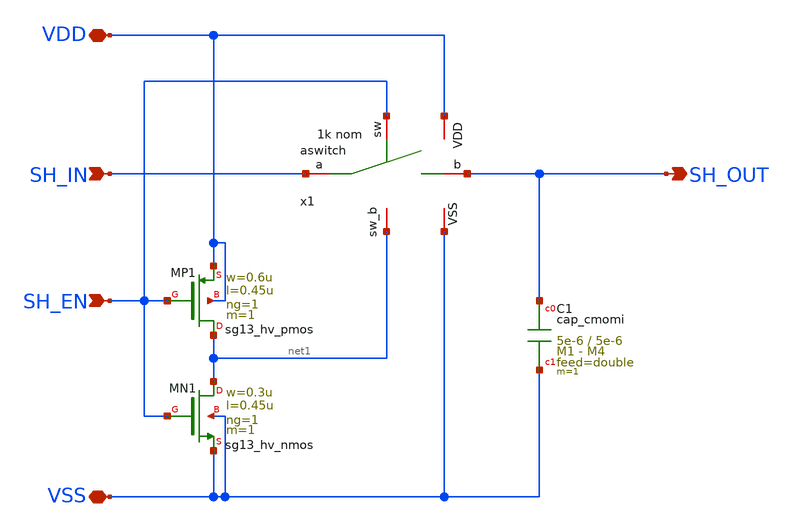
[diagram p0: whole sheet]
** sch_path: macros/heichips26_analog_project/macros/sample_and_hold/schematic/xschem/sample_and_hold.sch
**.subckt sample_and_hold SH_IN SH_EN VDD SH_OUT VSS
*.ipin SH_IN
*.ipin SH_EN
*.iopin VDD
*.opin SH_OUT
*.iopin VSS
x1 net1 VDD SH_OUT SH_IN VSS SH_EN aswitch
XC1 SH_OUT VSS cap_cmomi w=5e-6 l=5e-6 mmin=1 mmax=4 feed=double subblock=0 m=1 mm_ok=1
XMP1 net1 SH_EN VDD VDD sg13_hv_pmos w=0.6u l=0.45u ng=1 m=1 mm_ok=1
XMN1 net1 SH_EN VSS VSS sg13_hv_nmos w=0.3u l=0.45u ng=1 m=1 mm_ok=1
**.ends
.end
